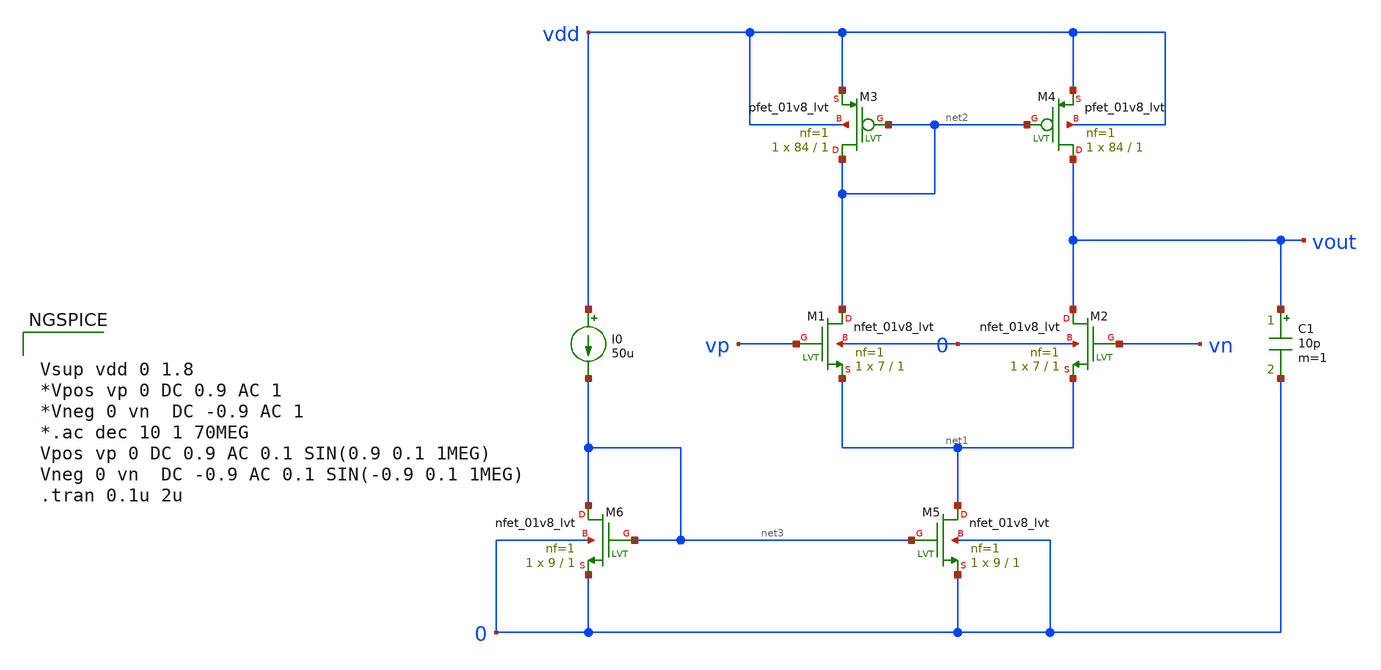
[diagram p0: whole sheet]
** sch_path: Analog_Blocks/OTA/Schematic/five_T_OTA.sch
**.subckt five_T_OTA
I0 vdd net3 50u
C1 vout 0 10p m=1
XM3 net2 net2 vdd vdd sky130_fd_pr__pfet_01v8_lvt L=1 W=84 nf=1 ad='int((nf+1)/2) * W/nf * 0.29' as='int((nf+2)/2) * W/nf * 0.29'
+ pd='2*int((nf+1)/2) * (W/nf + 0.29)' ps='2*int((nf+2)/2) * (W/nf + 0.29)' nrd='0.29 / W' nrs='0.29 / W'
+ sa=0 sb=0 sd=0 mult=1 m=1
XM4 vout net2 vdd vdd sky130_fd_pr__pfet_01v8_lvt L=1 W=84 nf=1 ad='int((nf+1)/2) * W/nf * 0.29' as='int((nf+2)/2) * W/nf * 0.29'
+ pd='2*int((nf+1)/2) * (W/nf + 0.29)' ps='2*int((nf+2)/2) * (W/nf + 0.29)' nrd='0.29 / W' nrs='0.29 / W'
+ sa=0 sb=0 sd=0 mult=1 m=1
XM1 net2 vp net1 0 sky130_fd_pr__nfet_01v8_lvt L=1 W=7 nf=1 ad='int((nf+1)/2) * W/nf * 0.29' as='int((nf+2)/2) * W/nf * 0.29'
+ pd='2*int((nf+1)/2) * (W/nf + 0.29)' ps='2*int((nf+2)/2) * (W/nf + 0.29)' nrd='0.29 / W' nrs='0.29 / W'
+ sa=0 sb=0 sd=0 mult=1 m=1
XM2 vout vn net1 0 sky130_fd_pr__nfet_01v8_lvt L=1 W=7 nf=1 ad='int((nf+1)/2) * W/nf * 0.29' as='int((nf+2)/2) * W/nf * 0.29'
+ pd='2*int((nf+1)/2) * (W/nf + 0.29)' ps='2*int((nf+2)/2) * (W/nf + 0.29)' nrd='0.29 / W' nrs='0.29 / W'
+ sa=0 sb=0 sd=0 mult=1 m=1
XM5 net1 net3 0 0 sky130_fd_pr__nfet_01v8_lvt L=1 W=9 nf=1 ad='int((nf+1)/2) * W/nf * 0.29' as='int((nf+2)/2) * W/nf * 0.29'
+ pd='2*int((nf+1)/2) * (W/nf + 0.29)' ps='2*int((nf+2)/2) * (W/nf + 0.29)' nrd='0.29 / W' nrs='0.29 / W'
+ sa=0 sb=0 sd=0 mult=1 m=1
XM6 net3 net3 0 0 sky130_fd_pr__nfet_01v8_lvt L=1 W=9 nf=1 ad='int((nf+1)/2) * W/nf * 0.29' as='int((nf+2)/2) * W/nf * 0.29'
+ pd='2*int((nf+1)/2) * (W/nf + 0.29)' ps='2*int((nf+2)/2) * (W/nf + 0.29)' nrd='0.29 / W' nrs='0.29 / W'
+ sa=0 sb=0 sd=0 mult=1 m=1
**** begin user architecture code

.include $::SKYWATER_MODELS/cells/nfet_01v8/sky130_fd_pr__nfet_01v8__tt.corner.spice
.include $::SKYWATER_MODELS/cells/nfet_01v8_lvt/sky130_fd_pr__nfet_01v8_lvt__tt.corner.spice
.include $::SKYWATER_MODELS/cells/pfet_01v8/sky130_fd_pr__pfet_01v8__tt.corner.spice
.include $::SKYWATER_MODELS/cells/nfet_03v3_nvt/sky130_fd_pr__nfet_03v3_nvt__tt.corner.spice
.include $::SKYWATER_MODELS/cells/nfet_05v0_nvt/sky130_fd_pr__nfet_05v0_nvt__tt.corner.spice
.include $::SKYWATER_MODELS/cells/esd_nfet_01v8/sky130_fd_pr__esd_nfet_01v8__tt.corner.spice
.include $::SKYWATER_MODELS/cells/pfet_01v8_lvt/sky130_fd_pr__pfet_01v8_lvt__tt.corner.spice
.include $::SKYWATER_MODELS/cells/pfet_01v8_hvt/sky130_fd_pr__pfet_01v8_hvt__tt.corner.spice
.include $::SKYWATER_MODELS/cells/esd_pfet_g5v0d10v5/sky130_fd_pr__esd_pfet_g5v0d10v5__tt.corner.spice
.include $::SKYWATER_MODELS/cells/pfet_g5v0d10v5/sky130_fd_pr__pfet_g5v0d10v5__tt.corner.spice
.include $::SKYWATER_MODELS/cells/pfet_g5v0d16v0/sky130_fd_pr__pfet_g5v0d16v0__tt.corner.spice
.include $::SKYWATER_MODELS/cells/nfet_g5v0d10v5/sky130_fd_pr__nfet_g5v0d10v5__tt.corner.spice
.include $::SKYWATER_MODELS/cells/nfet_g5v0d16v0/sky130_fd_pr__nfet_g5v0d16v0__tt_discrete.corner.spice
.include $::SKYWATER_MODELS/cells/esd_nfet_g5v0d10v5/sky130_fd_pr__esd_nfet_g5v0d10v5__tt.corner.spice
.include $::SKYWATER_MODELS/models/corners/tt/nonfet.spice
* Mismatch parameters
.include $::SKYWATER_MODELS/cells/nfet_01v8/sky130_fd_pr__nfet_01v8__mismatch.corner.spice
.include $::SKYWATER_MODELS/cells/pfet_01v8/sky130_fd_pr__pfet_01v8__mismatch.corner.spice
.include $::SKYWATER_MODELS/cells/nfet_01v8_lvt/sky130_fd_pr__nfet_01v8_lvt__mismatch.corner.spice
.include $::SKYWATER_MODELS/cells/pfet_01v8_lvt/sky130_fd_pr__pfet_01v8_lvt__mismatch.corner.spice
.include $::SKYWATER_MODELS/cells/pfet_01v8_hvt/sky130_fd_pr__pfet_01v8_hvt__mismatch.corner.spice
.include $::SKYWATER_MODELS/cells/nfet_g5v0d10v5/sky130_fd_pr__nfet_g5v0d10v5__mismatch.corner.spice
.include $::SKYWATER_MODELS/cells/pfet_g5v0d10v5/sky130_fd_pr__pfet_g5v0d10v5__mismatch.corner.spice
.include $::SKYWATER_MODELS/cells/nfet_05v0_nvt/sky130_fd_pr__nfet_05v0_nvt__mismatch.corner.spice
.include $::SKYWATER_MODELS/cells/nfet_03v3_nvt/sky130_fd_pr__nfet_03v3_nvt__mismatch.corner.spice
* Resistor$::SKYWATER_MODELS/Capacitor
.include $::SKYWATER_MODELS/models/r+c/res_typical__cap_typical.spice
.include $::SKYWATER_MODELS/models/r+c/res_typical__cap_typical__lin.spice
* Special cells
.include $::SKYWATER_MODELS/models/corners/tt/specialized_cells.spice
* All models
.include $::SKYWATER_MODELS/models/all.spice
* Corner
.include $::SKYWATER_MODELS/models/corners/tt/rf.spice



Vsup vdd 0 1.8
*Vpos vp 0 DC 0.9 AC 1
*Vneg 0 vn  DC -0.9 AC 1
*.ac dec 10 1 70MEG
Vpos vp 0 DC 0.9 AC 0.1 SIN(0.9 0.1 1MEG)
Vneg 0 vn  DC -0.9 AC 0.1 SIN(-0.9 0.1 1MEG)
.tran 0.1u 2u


**** end user architecture code
**.ends
.end
